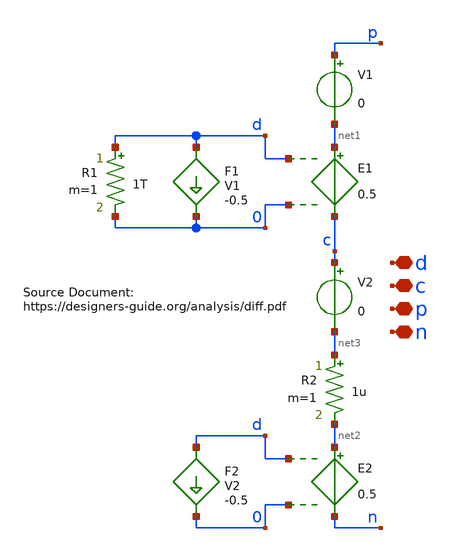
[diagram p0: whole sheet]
** sch_path: ITI_Labs/Lab6/Design/balun.sch
**.subckt balun p n d c
*.iopin p
*.iopin n
*.iopin d
*.iopin c
E1 net1 c d 0 0.5
V1 p net1 0
F1 d 0 V1 -0.5
R1 d 0 1T m=1
E2 net2 n d 0 0.5
V2 c net3 0
F2 d 0 V2 -0.5
R2 net3 net2 1u m=1
**.ends
.end
